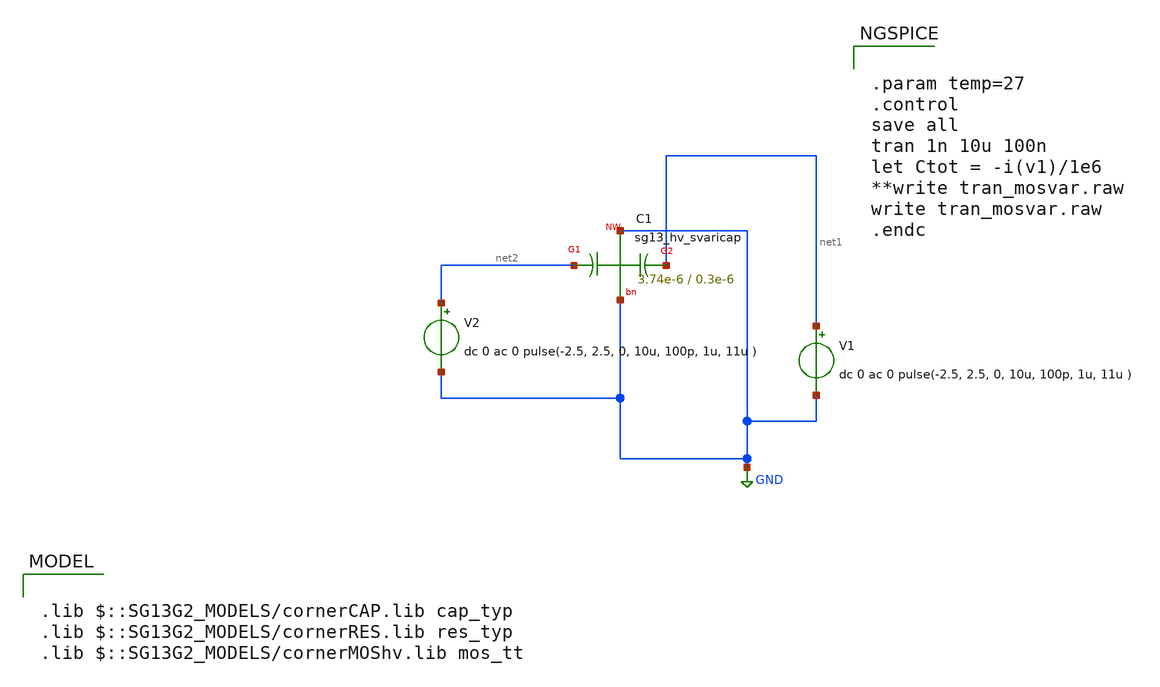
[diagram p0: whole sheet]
** sch_path: ihp-sg13g2/libs.tech/xschem/sg13g2_tests/tran_svaricap_test.sch
**.subckt tran_svaricap_test
XC1 net2 GND net1 GND sg13_hv_svaricap W=3.74e-6 L=0.3e-6 Nx=1
V1 net1 GND dc 0 ac 0 pulse(-2.5, 2.5, 0, 10u, 100p, 1u, 11u )
V2 net2 GND dc 0 ac 0 pulse(-2.5, 2.5, 0, 10u, 100p, 1u, 11u )
**** begin user architecture code

.lib $::SG13G2_MODELS/cornerCAP.lib cap_typ
.lib $::SG13G2_MODELS/cornerRES.lib res_typ
.lib $::SG13G2_MODELS/cornerMOShv.lib mos_tt



.param temp=27
.control
save all
tran 1n 10u 100n
let Ctot = -i(v1)/1e6
**write tran_mosvar.raw
write tran_mosvar.raw
.endc


**** end user architecture code
**.ends
.GLOBAL GND
.end
